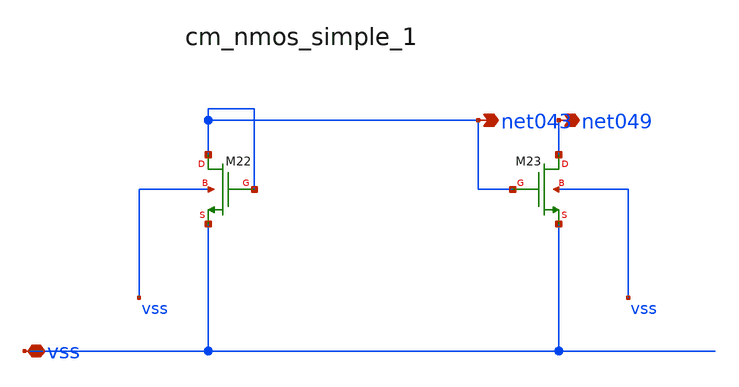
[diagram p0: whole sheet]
** sch_path: analog-db/raw/amp_006_leung_dfcfc1/hier/blocks/cm_nmos_simple_1.sch
**.subckt cm_nmos_simple_1 vss net043 net049
*.iopin vss
*.opin net043
*.opin net049
XM22 net043 net043 vss vss sg13_lv_nmos w=x_dut_xm22_w l=x_dut_xm22_l ng=1 m=x_dut_xm22_m
XM23 net049 net043 vss vss sg13_lv_nmos w=x_dut_xm23_w l=x_dut_xm23_l ng=1 m=x_dut_xm23_m
**.ends
.end
